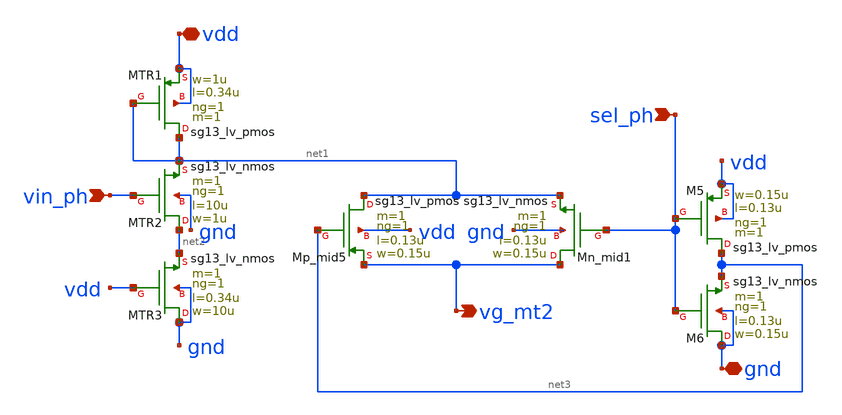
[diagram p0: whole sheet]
** sch_path: Enfoque_B/xschem/celdas/vi_ph_sel.sch
**.subckt vi_ph_sel vdd gnd vg_mt2 vin_ph sel_ph
*.iopin vdd
*.iopin gnd
*.opin vg_mt2
*.ipin vin_ph
*.ipin sel_ph
XMTR1 net1 net1 vdd vdd sg13_lv_pmos w=1u l=0.34u ng=1 m=1 mm_ok=1
XMTR2 net2 vin_ph net1 gnd sg13_lv_nmos w=1u l=10u ng=1 m=1 mm_ok=1
XMTR3 gnd vdd net2 gnd sg13_lv_nmos w=10u l=0.34u ng=1 m=1 mm_ok=1
XMn_mid1 vg_mt2 sel_ph net1 gnd sg13_lv_nmos w=0.15u l=0.13u ng=1 m=1 mm_ok=1
XMp_mid5 net1 net3 vg_mt2 vdd sg13_lv_pmos w=0.15u l=0.13u ng=1 m=1 mm_ok=1
XM5 net3 sel_ph vdd vdd sg13_lv_pmos w=0.15u l=0.13u ng=1 m=1 mm_ok=1
XM6 gnd sel_ph net3 gnd sg13_lv_nmos w=0.15u l=0.13u ng=1 m=1 mm_ok=1
**.ends
.end
